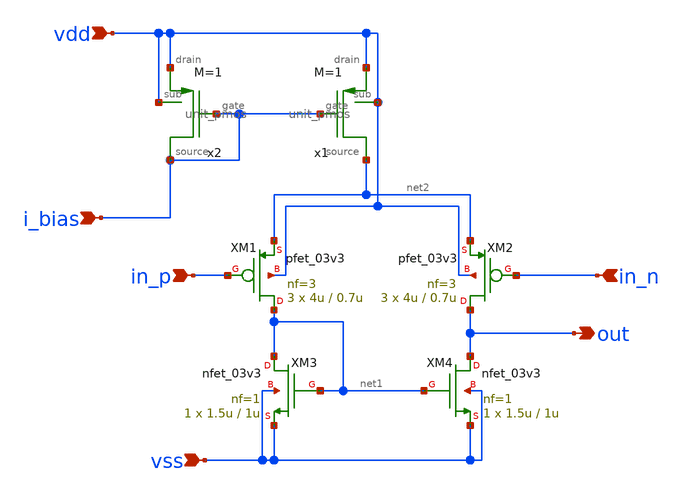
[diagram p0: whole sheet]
** sch_path: designs/libs/core_analog/ota_5t/ota_5t_P.sch
**.subckt ota_5t_P in_n i_bias vdd vss out in_p
*.ipin in_n
*.ipin i_bias
*.ipin vdd
*.ipin vss
*.opin out
*.ipin in_p
XM4 out net1 vss vss nfet_03v3 L=1u W=1.5u nf=1 ad='int((nf+1)/2) * W/nf * 0.18u' as='int((nf+2)/2) * W/nf * 0.18u'
+ pd='2*int((nf+1)/2) * (W/nf + 0.18u)' ps='2*int((nf+2)/2) * (W/nf + 0.18u)' nrd='0.18u / W' nrs='0.18u / W'
+ sa=0 sb=0 sd=0 m=1
XM3 net1 net1 vss vss nfet_03v3 L=1u W=1.5u nf=1 ad='int((nf+1)/2) * W/nf * 0.18u' as='int((nf+2)/2) * W/nf * 0.18u'
+ pd='2*int((nf+1)/2) * (W/nf + 0.18u)' ps='2*int((nf+2)/2) * (W/nf + 0.18u)' nrd='0.18u / W' nrs='0.18u / W'
+ sa=0 sb=0 sd=0 m=1
XM2 out in_n net2 vdd pfet_03v3 L=0.7u W=4u nf=3 ad='int((nf+1)/2) * W/nf * 0.18u' as='int((nf+2)/2) * W/nf * 0.18u'
+ pd='2*int((nf+1)/2) * (W/nf + 0.18u)' ps='2*int((nf+2)/2) * (W/nf + 0.18u)' nrd='0.18u / W' nrs='0.18u / W'
+ sa=0 sb=0 sd=0 m=3
XM1 net1 in_p net2 vdd pfet_03v3 L=0.7u W=4u nf=3 ad='int((nf+1)/2) * W/nf * 0.18u' as='int((nf+2)/2) * W/nf * 0.18u'
+ pd='2*int((nf+1)/2) * (W/nf + 0.18u)' ps='2*int((nf+2)/2) * (W/nf + 0.18u)' nrd='0.18u / W' nrs='0.18u / W'
+ sa=0 sb=0 sd=0 m=3
x2 vdd vdd i_bias i_bias unit_pmos M=1
x1 vdd vdd i_bias net2 unit_pmos M=1
**.ends

* expanding   symbol:  libs/core_analog/unit_pmos/unit_pmos.sym # of pins=4
** sym_path: libs/core_analog/unit_pmos/unit_pmos.sym
** sch_path: libs/core_analog/unit_pmos/unit_pmos.sch
.subckt unit_pmos drain sub gate source
*.iopin drain
*.iopin source
*.iopin sub
*.iopin gate
**** begin user architecture code

.param M=1

**** end user architecture code
XM3 drain gate source sub pfet_03v3 L=1u W=3.5u nf=1 ad='int((nf+1)/2) * W/nf * 0.18u' as='int((nf+2)/2) * W/nf * 0.18u'
+ pd='2*int((nf+1)/2) * (W/nf + 0.18u)' ps='2*int((nf+2)/2) * (W/nf + 0.18u)' nrd='0.18u / W' nrs='0.18u / W'
+ sa=0 sb=0 sd=0 m={M}
.ends

.end
